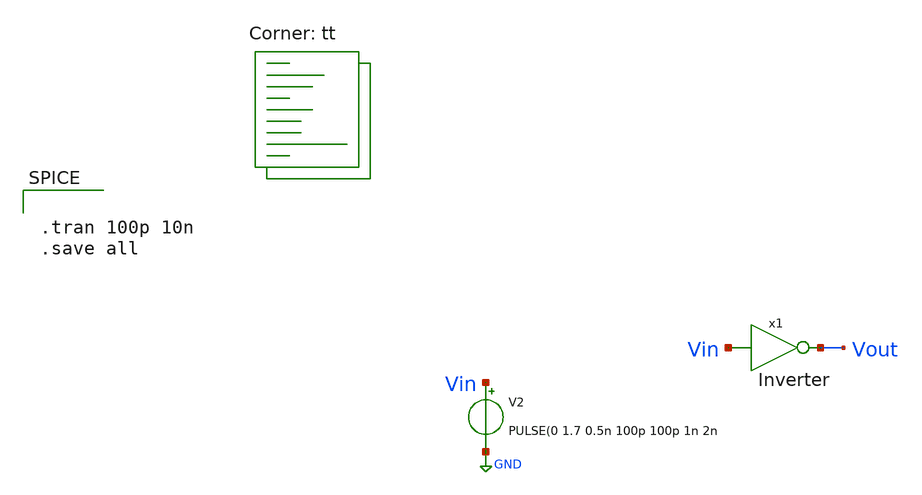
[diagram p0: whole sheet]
** sch_path: xschem/vault/Inverter_test.sch
**.subckt Inverter_test
x1 Vout Vin Inverter
V2 Vin GND PULSE(0 1.7 0.5n 100p 100p 1n 2n
**** begin user architecture code
.lib $::SKYWATER_MODELS/sky130.lib.spice tt


.tran 100p 10n
.save all





.control
tran 100p 10n
plot Vout



.endc




**** end user architecture code
**.ends

* expanding   symbol:  Inverter.sym # of pins=2
** sym_path: xschem/Inverter.sym
** sch_path: xschem/Inverter.sch
.subckt Inverter Vout Vin
*.ipin Vin
*.opin Vout
XM1 Vout Vin GND GND sky130_fd_pr__nfet_01v8 L=0.15 W=1 nf=1 ad='int((nf+1)/2) * W/nf * 0.29' as='int((nf+2)/2) * W/nf * 0.29'
+ pd='2*int((nf+1)/2) * (W/nf + 0.29)' ps='2*int((nf+2)/2) * (W/nf + 0.29)' nrd='0.29 / W' nrs='0.29 / W'
+ sa=0 sb=0 sd=0 mult=1 m=1
XM2 Vout Vin VDD VDD sky130_fd_pr__pfet_01v8 L=0.15 W=4 nf=1 ad='int((nf+1)/2) * W/nf * 0.29' as='int((nf+2)/2) * W/nf * 0.29'
+ pd='2*int((nf+1)/2) * (W/nf + 0.29)' ps='2*int((nf+2)/2) * (W/nf + 0.29)' nrd='0.29 / W' nrs='0.29 / W'
+ sa=0 sb=0 sd=0 mult=1 m=1
V1 VDD GND 1.8
.ends

.GLOBAL GND
.end
